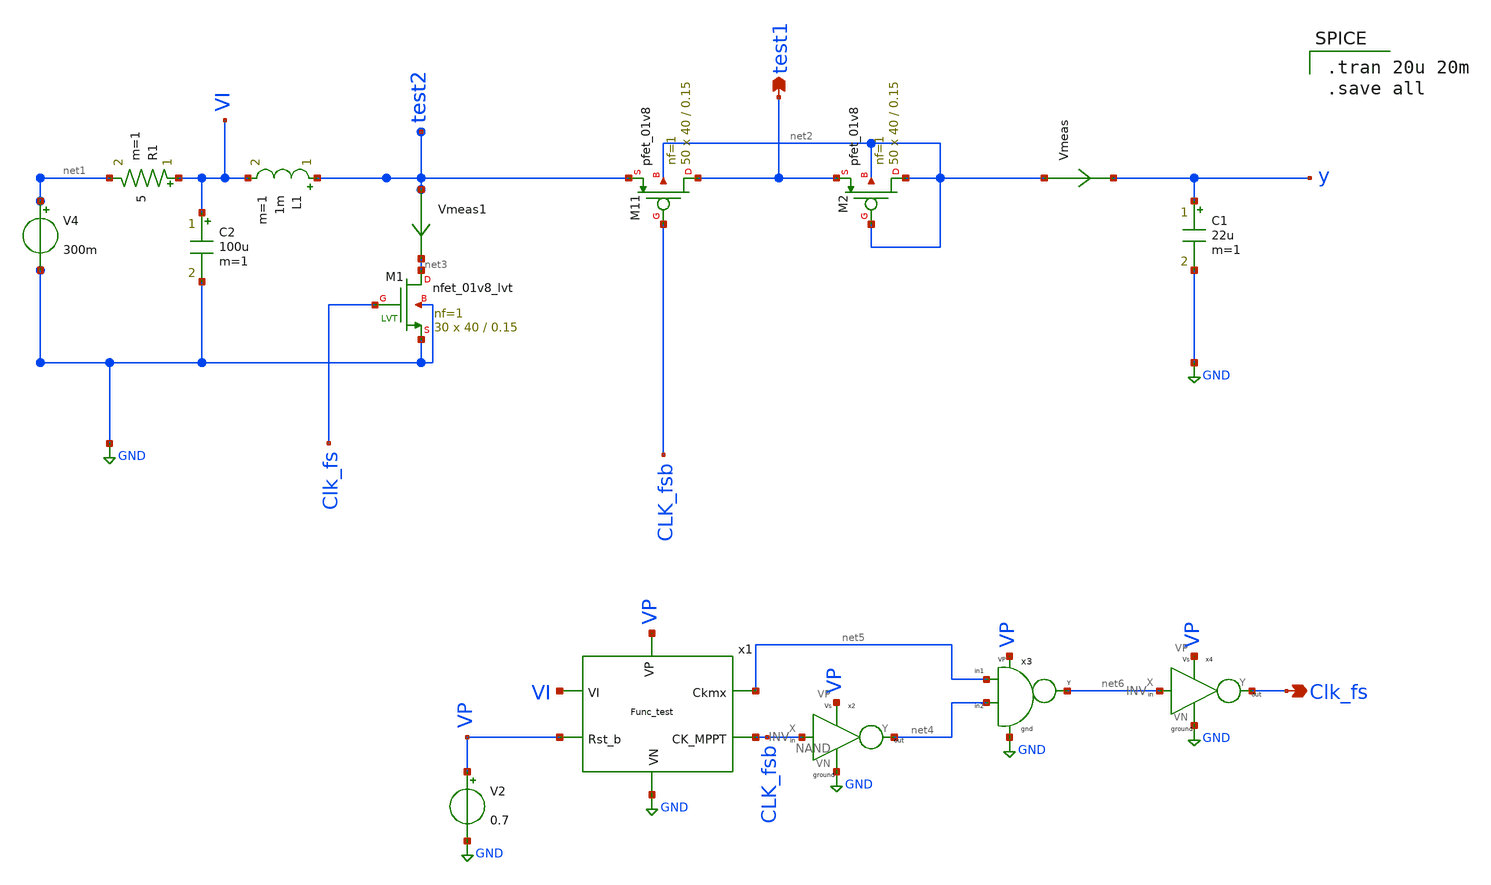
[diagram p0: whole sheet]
** sch_path: Blocks/MPPT/Functionality_test.sch
**.subckt Functionality_test test1 Clk_fs
*.opin test1
*.opin Clk_fs
C1 y GND 22u m=1
L1 test2 VI 1m m=1
XM11 test1 CLK_fsb test2 net2 sky130_fd_pr__pfet_01v8 L=0.15 W=40 nf=1 ad='int((nf+1)/2) * W/nf * 0.29'
+ as='int((nf+2)/2) * W/nf * 0.29' pd='2*int((nf+1)/2) * (W/nf + 0.29)' ps='2*int((nf+2)/2) * (W/nf + 0.29)'
+ nrd='0.29 / W' nrs='0.29 / W' sa=0 sb=0 sd=0 mult=50 m=50
Vmeas net2 y 0
.save i(vmeas)
Vmeas1 test2 net3 0
.save i(vmeas1)
XM2 net2 net2 test1 net2 sky130_fd_pr__pfet_01v8 L=0.15 W=40 nf=1 ad='int((nf+1)/2) * W/nf * 0.29' as='int((nf+2)/2) * W/nf * 0.29'
+ pd='2*int((nf+1)/2) * (W/nf + 0.29)' ps='2*int((nf+2)/2) * (W/nf + 0.29)' nrd='0.29 / W' nrs='0.29 / W'
+ sa=0 sb=0 sd=0 mult=50 m=50
XM1 net3 Clk_fs GND GND sky130_fd_pr__nfet_01v8_lvt L=0.15 W=40 nf=1 ad='int((nf+1)/2) * W/nf * 0.29'
+ as='int((nf+2)/2) * W/nf * 0.29' pd='2*int((nf+1)/2) * (W/nf + 0.29)' ps='2*int((nf+2)/2) * (W/nf + 0.29)'
+ nrd='0.29 / W' nrs='0.29 / W' sa=0 sb=0 sd=0 mult=30 m=30
R1 VI net1 5 m=1
C2 VI GND 100u m=1
x1 VI CLK_fsb net5 GND VP VP Func_test
x2 CLK_fsb net4 VP GND INV
x3 net4 net5 net6 VP GND NAND
x4 net6 Clk_fs VP GND INV
V2 VP GND 0.7
V4 net1 GND 300m
**** begin user architecture code

** opencircuitdesign pdks install
.lib $::SKYWATER_MODELS/sky130.lib.spice tt



.tran 20u 20m
.save all

**** end user architecture code
**.ends

* expanding   symbol:  pico_chipathon/Blocks/MPPT/Func_test.sym # of pins=6
** sym_path: Blocks/MPPT/Func_test.sym
** sch_path: Blocks/MPPT/Func_test.sch
.subckt Func_test VI CK_MPPT Ckmx VN Rst_b VP
*.ipin VI
*.ipin VP
*.ipin VN
*.ipin Rst_b
*.opin Ckmx
*.opin CK_MPPT
x1 VP net5 CK_MPPT Rst_b VN CK_MPPT1 CK_MPPT2 div8_copy
x2 net6 net5 VP VN Rst_b div32
x3 net7 CK_MPPT2 net4 Rst_b VN net11 VP net10 net8 net9 MPPT_Logic_Counter
x4 VP CK_MPPT1 VN net1 VI net11 net4 Conv_comp
R1 net1 net2 100k m=1
R2 net3 net1 100k m=1
C2 VI VN 0.1n m=1
C1 net1 VN 0.1n m=1
x5 net8 net7 net10 net9 VP VN net12 DCO
XM1 net3 CK_MPPT VN VN sky130_fd_pr__nfet_01v8_lvt L=0.15 W=0.42 nf=1 ad='int((nf+1)/2) * W/nf * 0.29'
+ as='int((nf+2)/2) * W/nf * 0.29' pd='2*int((nf+1)/2) * (W/nf + 0.29)' ps='2*int((nf+2)/2) * (W/nf + 0.29)'
+ nrd='0.29 / W' nrs='0.29 / W' sa=0 sb=0 sd=0 mult=50 m=50
XM2 net2 net13 VI VI sky130_fd_pr__pfet_01v8 L=0.15 W=1.26 nf=1 ad='int((nf+1)/2) * W/nf * 0.29' as='int((nf+2)/2) * W/nf * 0.29'
+ pd='2*int((nf+1)/2) * (W/nf + 0.29)' ps='2*int((nf+2)/2) * (W/nf + 0.29)' nrd='0.29 / W' nrs='0.29 / W'
+ sa=0 sb=0 sd=0 mult=50 m=50
x6 CK_MPPT net13 VP VN INV
x7 VP Ckmx net12 Rst_b VN div3
x8 Ckmx net6 VP VN Buff
.ends


* expanding   symbol:  pico_chipathon/component/INV/INV.sym # of pins=4
** sym_path: component/INV/INV.sym
** sch_path: component/INV/INV.sch
.subckt INV X Y VP VN
*.ipin X
*.opin Y
*.iopin VN
*.iopin VP
XM1 Y X VN VN sky130_fd_pr__nfet_01v8 L=0.15 W=0.42 nf=1 ad='int((nf+1)/2) * W/nf * 0.29' as='int((nf+2)/2) * W/nf * 0.29'
+ pd='2*int((nf+1)/2) * (W/nf + 0.29)' ps='2*int((nf+2)/2) * (W/nf + 0.29)' nrd='0.29 / W' nrs='0.29 / W'
+ sa=0 sb=0 sd=0 mult=1 m=1
XM2 Y X VP VP sky130_fd_pr__pfet_01v8 L=0.15 W=1.26 nf=1 ad='int((nf+1)/2) * W/nf * 0.29' as='int((nf+2)/2) * W/nf * 0.29'
+ pd='2*int((nf+1)/2) * (W/nf + 0.29)' ps='2*int((nf+2)/2) * (W/nf + 0.29)' nrd='0.29 / W' nrs='0.29 / W'
+ sa=0 sb=0 sd=0 mult=1 m=1
.ends


* expanding   symbol:  pico_chipathon/component/NAND2/NAND.sym # of pins=5
** sym_path: component/NAND2/NAND.sym
** sch_path: component/NAND2/NAND.sch
.subckt NAND B A Y VP VN
*.iopin VP
*.ipin A
*.ipin B
*.opin Y
*.iopin VN
XM1 Y A VP VP sky130_fd_pr__pfet_01v8 L=0.15 W=1.26 nf=1 ad='int((nf+1)/2) * W/nf * 0.29' as='int((nf+2)/2) * W/nf * 0.29'
+ pd='2*int((nf+1)/2) * (W/nf + 0.29)' ps='2*int((nf+2)/2) * (W/nf + 0.29)' nrd='0.29 / W' nrs='0.29 / W'
+ sa=0 sb=0 sd=0 mult=1 m=1
XM2 Y B VP VP sky130_fd_pr__pfet_01v8 L=0.15 W=1.26 nf=1 ad='int((nf+1)/2) * W/nf * 0.29' as='int((nf+2)/2) * W/nf * 0.29'
+ pd='2*int((nf+1)/2) * (W/nf + 0.29)' ps='2*int((nf+2)/2) * (W/nf + 0.29)' nrd='0.29 / W' nrs='0.29 / W'
+ sa=0 sb=0 sd=0 mult=1 m=1
XM3 Y A net1 net1 sky130_fd_pr__nfet_01v8 L=0.15 W=0.84 nf=1 ad='int((nf+1)/2) * W/nf * 0.29' as='int((nf+2)/2) * W/nf * 0.29'
+ pd='2*int((nf+1)/2) * (W/nf + 0.29)' ps='2*int((nf+2)/2) * (W/nf + 0.29)' nrd='0.29 / W' nrs='0.29 / W'
+ sa=0 sb=0 sd=0 mult=1 m=1
XM4 net1 B VN VN sky130_fd_pr__nfet_01v8 L=0.15 W=0.84 nf=1 ad='int((nf+1)/2) * W/nf * 0.29' as='int((nf+2)/2) * W/nf * 0.29'
+ pd='2*int((nf+1)/2) * (W/nf + 0.29)' ps='2*int((nf+2)/2) * (W/nf + 0.29)' nrd='0.29 / W' nrs='0.29 / W'
+ sa=0 sb=0 sd=0 mult=1 m=1
.ends


* expanding   symbol:  pico_chipathon/Blocks/MPPT/div8_copy.sym # of pins=7
** sym_path: Blocks/MPPT/div8_copy.sym
** sch_path: Blocks/MPPT/div8_copy.sch
.subckt div8_copy Vp Clk CK_MPPT RST_b Vn CK_MPPT1 CK_MPPT2
*.ipin Clk
*.ipin RST_b
*.opin CK_MPPT
*.opin CK_MPPT1
*.opin CK_MPPT2
*.ipin Vn
*.ipin Vp
x1 net2 Clk RST_b Vn Vp net1 net2 DFF1
x2 net3 net1 RST_b Vn Vp net4 net3 DFF1
x3 net6 net4 RST_b Vn Vp net5 net6 DFF1
x4 net7 CK_MPPT Vp Vn INV
x5 net8 CK_MPPT1 Vp Vn INV
x7 net9 CK_MPPT2 Vp Vn INV
x8 net1 net12 Vp Vn INV
x11 net4 net11 Vp Vn INV
x12 net4 net10 Vp Vn INV
x6 net5 net11 net12 Vp Vn net9 NAND3
x9 net5 net10 net1 Vp Vn net8 NAND3
x10 net5 net4 net1 Vp Vn net7 NAND3
.ends


* expanding   symbol:  pico_chipathon/Blocks/Divide by 32 ckt/div32.sym # of pins=5
** sym_path: Blocks/Divide by 32 ckt/div32.sym
** sch_path: Blocks/Divide by 32 ckt/div32.sch
.subckt div32 Clk Clk/32 VP VN RST_b
*.opin Clk/32
*.ipin Clk
*.iopin VP
*.iopin VN
*.ipin RST_b
x1 net2 Clk RST_b VN VP net1 net2 DFF1
x6 net9 net10 VN VP Buff
x2 net3 net1 RST_b VN VP net4 net3 DFF1
x3 net8 net4 RST_b VN VP net5 net8 DFF1
x4 net7 net5 RST_b VN VP net6 net7 DFF1
x5 net9 net6 RST_b VN VP Clk/32 net10 DFF1
.ends


* expanding   symbol:  pico_chipathon/Blocks/MPPT/MPPT_Logic_Counter.sym # of pins=10
** sym_path: Blocks/MPPT/MPPT_Logic_Counter.sym
** sch_path: Blocks/MPPT/MPPT_Logic_Counter.sch
.subckt MPPT_Logic_Counter QA Clk X_b Rst VN X VP QD QB QC
*.opin QD
*.ipin VP
*.opin QC
*.opin QB
*.opin QA
*.ipin VN
*.ipin X
*.ipin X_b
*.ipin Clk
*.ipin Rst
x4 net47 net46 net2 VP VN NAND
x5 QD X_b net38 VP VN NAND
x6 net51 net50 net3 VP VN NAND
x16 QA QD net29 VP VN NAND
x48 QB QD net31 VP VN NAND
x49 QC QD net32 VP VN NAND
x50 QD X net35 VP VN NAND
x52 net44 net43 net28 VP VN NAND
x54 VP net14 X_b QC QB_b QA_b VN nand4
x12 VP net15 X_b QD QB_b QA_b VN nand4
x15 VP net17 QD QC QB QA VN nand4
x22 VP net8 X QC_b QB QA VN nand4
x24 VP net36 X QC QB QA VN nand4
x17 VP net52 net53 net57 net50 VN nor3
x26 VP net54 net55 net56 net51 VN nor3
x56 VP net10 net11 net48 net46 VN nor3
x57 VP net49 net16 net18 net47 VN nor3
x25 VP net30 net33 net45 net43 VN nor3
x64 X_b QB QA VP VN net9 NAND3
x9 X QB_b QA VP VN net12 NAND3
x10 X QB QA_b VP VN net13 NAND3
x11 X_b QC QA VP VN net4 NAND3
x13 QC QB QA_b VP VN net5 NAND3
x14 QD QC QA VP VN net6 NAND3
x19 X QC QB_b VP VN net7 NAND3
x20 QC_b QB_b QA_b VP VN net39 NAND3
x23 VP net34 net37 net44 VN NOR2
x8 VP net38 net39 net56 VN NOR2
x1 net2 Clk Rst VN VP QB QB_b DFF1
x18 net3 Clk Rst VN VP QC QC_b DFF1
x29 net28 Clk Rst VN VP QD DFF
x32 net17 net18 VP VN INV
x38 net15 net16 VP VN INV
x39 net14 net49 VP VN INV
x40 net13 net48 VP VN INV
x42 net9 net10 VP VN INV
x43 net12 net11 VP VN INV
x31 net8 net55 VP VN INV
x33 net7 net54 VP VN INV
x36 net6 net57 VP VN INV
x37 net5 net53 VP VN INV
x41 net4 net52 VP VN INV
x34 net29 net30 VP VN INV
x44 net31 net33 VP VN INV
x51 net32 net45 VP VN INV
x53 net35 net34 VP VN INV
x55 net36 net37 VP VN INV
x35 net1 Clk Rst VN VP QA QA_b DFF1
x58 VP net20 net23 net42 net40 VN nor3
x59 VP net40 net41 net1 VN NOR2
x3 net27 net24 net41 VP VN NAND
x21 net19 net20 VP VN INV
x27 net21 net23 VP VN INV
x28 net22 net42 VP VN INV
x30 net25 net24 VP VN INV
x2 net26 net27 VP VN INV
x60 VP net26 X QD QC QB VN nand4
x7 QA_b QB net19 VP VN NAND
x45 QA_b QC net21 VP VN NAND
x46 QA_b QD net22 VP VN NAND
x47 QA_b X net25 VP VN NAND
.ends


* expanding   symbol:  pico_chipathon/Blocks/Conv_comparator/Conv_comp.sym # of pins=7
** sym_path: Blocks/Conv_comparator/Conv_comp.sym
** sch_path: Blocks/Conv_comparator/Conv_comp.sch
.subckt Conv_comp Vdd Clk VN Vin- Vin+ Out+ Out-
*.iopin Vin+
*.iopin Vin-
*.iopin Out+
*.iopin Out-
*.ipin VN
*.ipin Vdd
*.ipin Clk
XM6 net1 Clk Vdd Vdd sky130_fd_pr__pfet_01v8 L=0.15 W=1.26 nf=1 ad='int((nf+1)/2) * W/nf * 0.29' as='int((nf+2)/2) * W/nf * 0.29'
+ pd='2*int((nf+1)/2) * (W/nf + 0.29)' ps='2*int((nf+2)/2) * (W/nf + 0.29)' nrd='0.29 / W' nrs='0.29 / W'
+ sa=0 sb=0 sd=0 mult=1 m=1
XM7 O1- Vin+ net1 Vdd sky130_fd_pr__pfet_01v8 L=0.15 W=1.26 nf=1 ad='int((nf+1)/2) * W/nf * 0.29' as='int((nf+2)/2) * W/nf * 0.29'
+ pd='2*int((nf+1)/2) * (W/nf + 0.29)' ps='2*int((nf+2)/2) * (W/nf + 0.29)' nrd='0.29 / W' nrs='0.29 / W'
+ sa=0 sb=0 sd=0 mult=1 m=1
XM8 O1+ Vin- net1 Vdd sky130_fd_pr__pfet_01v8 L=0.15 W=1.26 nf=1 ad='int((nf+1)/2) * W/nf * 0.29' as='int((nf+2)/2) * W/nf * 0.29'
+ pd='2*int((nf+1)/2) * (W/nf + 0.29)' ps='2*int((nf+2)/2) * (W/nf + 0.29)' nrd='0.29 / W' nrs='0.29 / W'
+ sa=0 sb=0 sd=0 mult=1 m=1
XM5 O1- Clk VN VN sky130_fd_pr__nfet_01v8 L=0.15 W=0.42 nf=1 ad='int((nf+1)/2) * W/nf * 0.29' as='int((nf+2)/2) * W/nf * 0.29'
+ pd='2*int((nf+1)/2) * (W/nf + 0.29)' ps='2*int((nf+2)/2) * (W/nf + 0.29)' nrd='0.29 / W' nrs='0.29 / W'
+ sa=0 sb=0 sd=0 mult=1 m=1
XM21 O1+ Clk VN VN sky130_fd_pr__nfet_01v8 L=0.15 W=0.42 nf=1 ad='int((nf+1)/2) * W/nf * 0.29' as='int((nf+2)/2) * W/nf * 0.29'
+ pd='2*int((nf+1)/2) * (W/nf + 0.29)' ps='2*int((nf+2)/2) * (W/nf + 0.29)' nrd='0.29 / W' nrs='0.29 / W'
+ sa=0 sb=0 sd=0 mult=1 m=1
XM1 O2- Clk_b Vdd Vdd sky130_fd_pr__pfet_01v8 L=0.15 W=1.26 nf=1 ad='int((nf+1)/2) * W/nf * 0.29' as='int((nf+2)/2) * W/nf * 0.29'
+ pd='2*int((nf+1)/2) * (W/nf + 0.29)' ps='2*int((nf+2)/2) * (W/nf + 0.29)' nrd='0.29 / W' nrs='0.29 / W'
+ sa=0 sb=0 sd=0 mult=1 m=1
XM2 O2- O2+ Vdd Vdd sky130_fd_pr__pfet_01v8 L=0.15 W=1.26 nf=1 ad='int((nf+1)/2) * W/nf * 0.29' as='int((nf+2)/2) * W/nf * 0.29'
+ pd='2*int((nf+1)/2) * (W/nf + 0.29)' ps='2*int((nf+2)/2) * (W/nf + 0.29)' nrd='0.29 / W' nrs='0.29 / W'
+ sa=0 sb=0 sd=0 mult=1 m=1
XM3 O2+ O2- Vdd Vdd sky130_fd_pr__pfet_01v8 L=0.15 W=1.26 nf=1 ad='int((nf+1)/2) * W/nf * 0.29' as='int((nf+2)/2) * W/nf * 0.29'
+ pd='2*int((nf+1)/2) * (W/nf + 0.29)' ps='2*int((nf+2)/2) * (W/nf + 0.29)' nrd='0.29 / W' nrs='0.29 / W'
+ sa=0 sb=0 sd=0 mult=1 m=1
XM4 O2+ Clk_b Vdd Vdd sky130_fd_pr__pfet_01v8 L=0.15 W=1.26 nf=1 ad='int((nf+1)/2) * W/nf * 0.29' as='int((nf+2)/2) * W/nf * 0.29'
+ pd='2*int((nf+1)/2) * (W/nf + 0.29)' ps='2*int((nf+2)/2) * (W/nf + 0.29)' nrd='0.29 / W' nrs='0.29 / W'
+ sa=0 sb=0 sd=0 mult=1 m=1
XM9 net3 O1- O2- VN sky130_fd_pr__nfet_01v8 L=0.15 W=0.42 nf=1 ad='int((nf+1)/2) * W/nf * 0.29' as='int((nf+2)/2) * W/nf * 0.29'
+ pd='2*int((nf+1)/2) * (W/nf + 0.29)' ps='2*int((nf+2)/2) * (W/nf + 0.29)' nrd='0.29 / W' nrs='0.29 / W'
+ sa=0 sb=0 sd=0 mult=1 m=1
XM10 net2 O1+ O2+ VN sky130_fd_pr__nfet_01v8 L=0.15 W=0.42 nf=1 ad='int((nf+1)/2) * W/nf * 0.29' as='int((nf+2)/2) * W/nf * 0.29'
+ pd='2*int((nf+1)/2) * (W/nf + 0.29)' ps='2*int((nf+2)/2) * (W/nf + 0.29)' nrd='0.29 / W' nrs='0.29 / W'
+ sa=0 sb=0 sd=0 mult=1 m=1
XM11 VN O2+ net3 VN sky130_fd_pr__nfet_01v8 L=0.15 W=0.42 nf=1 ad='int((nf+1)/2) * W/nf * 0.29' as='int((nf+2)/2) * W/nf * 0.29'
+ pd='2*int((nf+1)/2) * (W/nf + 0.29)' ps='2*int((nf+2)/2) * (W/nf + 0.29)' nrd='0.29 / W' nrs='0.29 / W'
+ sa=0 sb=0 sd=0 mult=1 m=1
XM12 VN O2- net2 VN sky130_fd_pr__nfet_01v8 L=0.15 W=0.42 nf=1 ad='int((nf+1)/2) * W/nf * 0.29' as='int((nf+2)/2) * W/nf * 0.29'
+ pd='2*int((nf+1)/2) * (W/nf + 0.29)' ps='2*int((nf+2)/2) * (W/nf + 0.29)' nrd='0.29 / W' nrs='0.29 / W'
+ sa=0 sb=0 sd=0 mult=1 m=1
x1 Clk Clk_b Vdd VN INV
x2 O2+ net4 Vdd VN INV
x3 O2- net5 Vdd VN INV
x4 net4 Clk Vdd VN Vdd Out+ DFF
x5 net5 Clk Vdd VN Vdd Out- DFF
.ends


* expanding   symbol:  pico_chipathon/Blocks/DCO/DCO.sym # of pins=7
** sym_path: Blocks/DCO/DCO.sym
** sch_path: Blocks/DCO/DCO.sch
.subckt DCO Y1 Y0 Y3 Y2 VS VN Out
*.ipin VS
*.opin Out
*.ipin VN
*.iopin Y3
*.iopin Y2
*.iopin Y1
*.iopin Y0
C1 net38 VN 5f m=1
C2 net39 VN 5f m=1
C3 net40 VN 5f m=1
C4 net41 VN 5f m=1
XM1 net16 L0 net38 VN sky130_fd_pr__nfet_01v8 L=0.15 W=5 nf=1 ad='int((nf+1)/2) * W/nf * 0.29' as='int((nf+2)/2) * W/nf * 0.29'
+ pd='2*int((nf+1)/2) * (W/nf + 0.29)' ps='2*int((nf+2)/2) * (W/nf + 0.29)' nrd='0.29 / W' nrs='0.29 / W'
+ sa=0 sb=0 sd=0 mult=1 m=1
XM2 net17 L1 net39 VN sky130_fd_pr__nfet_01v8 L=0.15 W=5 nf=1 ad='int((nf+1)/2) * W/nf * 0.29' as='int((nf+2)/2) * W/nf * 0.29'
+ pd='2*int((nf+1)/2) * (W/nf + 0.29)' ps='2*int((nf+2)/2) * (W/nf + 0.29)' nrd='0.29 / W' nrs='0.29 / W'
+ sa=0 sb=0 sd=0 mult=1 m=1
XM3 net18 L2 net40 VN sky130_fd_pr__nfet_01v8 L=0.15 W=5 nf=1 ad='int((nf+1)/2) * W/nf * 0.29' as='int((nf+2)/2) * W/nf * 0.29'
+ pd='2*int((nf+1)/2) * (W/nf + 0.29)' ps='2*int((nf+2)/2) * (W/nf + 0.29)' nrd='0.29 / W' nrs='0.29 / W'
+ sa=0 sb=0 sd=0 mult=1 m=1
XM4 net19 L3 net41 VN sky130_fd_pr__nfet_01v8 L=0.15 W=5 nf=1 ad='int((nf+1)/2) * W/nf * 0.29' as='int((nf+2)/2) * W/nf * 0.29'
+ pd='2*int((nf+1)/2) * (W/nf + 0.29)' ps='2*int((nf+2)/2) * (W/nf + 0.29)' nrd='0.29 / W' nrs='0.29 / W'
+ sa=0 sb=0 sd=0 mult=1 m=1
XM5 net33 H0 net17 VN sky130_fd_pr__nfet_01v8 L=0.15 W=10 nf=1 ad='int((nf+1)/2) * W/nf * 0.29' as='int((nf+2)/2) * W/nf * 0.29'
+ pd='2*int((nf+1)/2) * (W/nf + 0.29)' ps='2*int((nf+2)/2) * (W/nf + 0.29)' nrd='0.29 / W' nrs='0.29 / W'
+ sa=0 sb=0 sd=0 mult=1 m=1
XM6 net33 H1 net19 VN sky130_fd_pr__nfet_01v8 L=0.15 W=10 nf=1 ad='int((nf+1)/2) * W/nf * 0.29' as='int((nf+2)/2) * W/nf * 0.29'
+ pd='2*int((nf+1)/2) * (W/nf + 0.29)' ps='2*int((nf+2)/2) * (W/nf + 0.29)' nrd='0.29 / W' nrs='0.29 / W'
+ sa=0 sb=0 sd=0 mult=1 m=1
XM7 net33 H2 net21 VN sky130_fd_pr__nfet_01v8 L=0.15 W=10 nf=1 ad='int((nf+1)/2) * W/nf * 0.29' as='int((nf+2)/2) * W/nf * 0.29'
+ pd='2*int((nf+1)/2) * (W/nf + 0.29)' ps='2*int((nf+2)/2) * (W/nf + 0.29)' nrd='0.29 / W' nrs='0.29 / W'
+ sa=0 sb=0 sd=0 mult=1 m=1
XM9 net33 net36 net17 VS sky130_fd_pr__pfet_01v8 L=0.15 W=3 nf=1 ad='int((nf+1)/2) * W/nf * 0.29' as='int((nf+2)/2) * W/nf * 0.29'
+ pd='2*int((nf+1)/2) * (W/nf + 0.29)' ps='2*int((nf+2)/2) * (W/nf + 0.29)' nrd='0.29 / W' nrs='0.29 / W'
+ sa=0 sb=0 sd=0 mult=1 m=1
XM10 net33 net34 net19 VS sky130_fd_pr__pfet_01v8 L=0.15 W=3 nf=1 ad='int((nf+1)/2) * W/nf * 0.29' as='int((nf+2)/2) * W/nf * 0.29'
+ pd='2*int((nf+1)/2) * (W/nf + 0.29)' ps='2*int((nf+2)/2) * (W/nf + 0.29)' nrd='0.29 / W' nrs='0.29 / W'
+ sa=0 sb=0 sd=0 mult=1 m=1
XM11 net33 net35 net21 VS sky130_fd_pr__pfet_01v8 L=0.15 W=3 nf=1 ad='int((nf+1)/2) * W/nf * 0.29' as='int((nf+2)/2) * W/nf * 0.29'
+ pd='2*int((nf+1)/2) * (W/nf + 0.29)' ps='2*int((nf+2)/2) * (W/nf + 0.29)' nrd='0.29 / W' nrs='0.29 / W'
+ sa=0 sb=0 sd=0 mult=1 m=1
XM8 net33 net37 Out VS sky130_fd_pr__pfet_01v8 L=0.15 W=3 nf=1 ad='int((nf+1)/2) * W/nf * 0.29' as='int((nf+2)/2) * W/nf * 0.29'
+ pd='2*int((nf+1)/2) * (W/nf + 0.29)' ps='2*int((nf+2)/2) * (W/nf + 0.29)' nrd='0.29 / W' nrs='0.29 / W'
+ sa=0 sb=0 sd=0 mult=1 m=1
XM12 net33 H3 Out VN sky130_fd_pr__nfet_01v8 L=0.15 W=10 nf=1 ad='int((nf+1)/2) * W/nf * 0.29' as='int((nf+2)/2) * W/nf * 0.29'
+ pd='2*int((nf+1)/2) * (W/nf + 0.29)' ps='2*int((nf+2)/2) * (W/nf + 0.29)' nrd='0.29 / W' nrs='0.29 / W'
+ sa=0 sb=0 sd=0 mult=1 m=1
XM13 net16 net45 net38 VS sky130_fd_pr__pfet_01v8 L=0.15 W=3 nf=1 ad='int((nf+1)/2) * W/nf * 0.29' as='int((nf+2)/2) * W/nf * 0.29'
+ pd='2*int((nf+1)/2) * (W/nf + 0.29)' ps='2*int((nf+2)/2) * (W/nf + 0.29)' nrd='0.29 / W' nrs='0.29 / W'
+ sa=0 sb=0 sd=0 mult=1 m=1
XM14 net17 net44 net39 VS sky130_fd_pr__pfet_01v8 L=0.15 W=3 nf=1 ad='int((nf+1)/2) * W/nf * 0.29' as='int((nf+2)/2) * W/nf * 0.29'
+ pd='2*int((nf+1)/2) * (W/nf + 0.29)' ps='2*int((nf+2)/2) * (W/nf + 0.29)' nrd='0.29 / W' nrs='0.29 / W'
+ sa=0 sb=0 sd=0 mult=1 m=1
XM15 net18 net42 net40 VS sky130_fd_pr__pfet_01v8 L=0.15 W=3 nf=1 ad='int((nf+1)/2) * W/nf * 0.29' as='int((nf+2)/2) * W/nf * 0.29'
+ pd='2*int((nf+1)/2) * (W/nf + 0.29)' ps='2*int((nf+2)/2) * (W/nf + 0.29)' nrd='0.29 / W' nrs='0.29 / W'
+ sa=0 sb=0 sd=0 mult=1 m=1
XM16 net19 net43 net41 VS sky130_fd_pr__pfet_01v8 L=0.15 W=3 nf=1 ad='int((nf+1)/2) * W/nf * 0.29' as='int((nf+2)/2) * W/nf * 0.29'
+ pd='2*int((nf+1)/2) * (W/nf + 0.29)' ps='2*int((nf+2)/2) * (W/nf + 0.29)' nrd='0.29 / W' nrs='0.29 / W'
+ sa=0 sb=0 sd=0 mult=1 m=1
x9 Y3 net1 VS VN INV_a
x10 net46 H0 VS VN INV_a
x11 net47 H1 VS VN INV_a
x13 net48 H2 VS VN INV_a
x15 net49 H3 VS VN INV_a
x17 Y2 net4 VS VN INV_a
x18 Y3 net3 VS VN INV_a
x19 Y2 net2 VS VN INV_a
x23 H3 net37 VS VN INV_a
x3 H2 net35 VS VN INV_a
x2 H1 net34 VS VN INV_a
x1 H0 net36 VS VN INV_a
x4 L0 net45 VS VN INV_a
x20 L1 net44 VS VN INV_a
x5 L2 net42 VS VN INV_a
x6 L3 net43 VS VN INV_a
x7 Y1 net11 VS VN INV_a
x8 net50 net9 VS VN INV_a
x21 net51 net10 VS VN INV_a
x22 net52 L0 VS VN INV_a
x24 net53 net12 VS VN INV_a
x26 Y0 net14 VS VN INV_a
x34 net54 net13 VS VN INV_a
x28 net55 L1 VS VN INV_a
x36 Y0 net11 net50 VS VN NAND
x38 net14 Y1 net53 VS VN NAND
x33 Y0 Y1 net51 VS VN NAND
x37 net6 net5 net52 VS VN NAND
x25 net8 net7 net55 VS VN NAND
x27 Y0 Y1 net54 VS VN NAND
x39 Y1 net29 VS VN INV_a
x40 net56 net27 VS VN INV_a
x41 net57 net30 VS VN INV_a
x42 net58 L3 VS VN INV_a
x43 net59 L2 VS VN INV_a
x44 net60 net31 VS VN INV_a
x55 Y0 net32 VS VN INV_a
x59 net61 net28 VS VN INV_a
x62 Y0 net29 net56 VS VN NAND
x63 Y0 Y1 net61 VS VN NAND
x64 net32 Y1 net57 VS VN NAND
x65 Y0 Y1 net60 VS VN NAND
x66 net24 net23 net59 VS VN NAND
x67 net26 net25 net58 VS VN NAND
x54 net31 net30 net25 VS VN OR_2
x58 H3 H2 net26 VS VN OR_2
x60 net28 net27 net23 VS VN OR_2
x68 H3 H2 net24 VS VN OR_2
x32 H1 H0 net8 VS VN OR_2
x31 net13 net12 net7 VS VN OR_2
x56 H1 H0 net6 VS VN OR_2
x30 net10 net9 net5 VS VN OR_2
x29 net2 net1 net46 VS VN NAND
x57 net3 Y2 net47 VS VN NAND
x61 net4 Y3 net48 VS VN NAND
x69 Y2 Y3 net49 VS VN NAND
x12 net33 net15 VS VN Redn_INV
x14 net15 net16 VS VN Redn_INV
x16 net16 net17 VS VN Redn_INV
x35 net17 net18 VS VN Redn_INV
x53 net18 net19 VS VN Redn_INV
x70 net19 net20 VS VN Redn_INV
x71 net20 net21 VS VN Redn_INV
x72 net21 net22 VS VN Redn_INV
x73 net22 Out VS VN Redn_INV
.ends


* expanding   symbol:  pico_chipathon/Blocks/Divide by 3 Circuit/div3.sym # of pins=5
** sym_path: Blocks/Divide by 3 Circuit/div3.sym
** sch_path: Blocks/Divide by 3 Circuit/div3.sch
.subckt div3 VP Clk/3 Clk RST_b VN
*.opin Clk/3
*.ipin Clk
*.ipin VN
*.ipin RST_b
*.ipin VP
x3 net2 Clk RST_b VN VP net3 net5 DFF1
x8 Clk net1 VP VN INV
x1 net8 net2 VP VN INV
x9 net6 net5 net8 VP VN NAND
x2 net7 net4 Clk/3 VP VN OR_2
x7 net3 Clk RST_b VN VP net4 net6 DFF1
x10 net4 net1 RST_b VN VP net7 net9 DFF1
.ends


* expanding   symbol:  pico_chipathon/Blocks/Buffer/Buff.sym # of pins=4
** sym_path: Blocks/Buffer/Buff.sym
** sch_path: Blocks/Buffer/Buff.sch
.subckt Buff X Y VP VN
*.ipin X
*.opin Y
*.iopin VN
*.iopin VP
x1 X net1 VP VN INV
x2 net1 Y VP VN INV
.ends


* expanding   symbol:  component/FlipFlops/DFF1.sym # of pins=7
** sym_path: component/FlipFlops/DFF1.sym
** sch_path: component/FlipFlops/DFF1.sch
.subckt DFF1 D Clk RST VN VP Q Qb
*.opin Q
*.iopin VN
*.iopin VP
*.ipin Clk
*.ipin D
*.ipin RST
*.opin Qb
x7 net2 net4 net3 VP VN NAND
x8 net3 Clk RST VP VN net2 NAND3
x6 Q net1 RST VP VN Qb NAND3
x4 net2 Clk net4 VP VN net1 NAND3
x5 net1 D RST VP VN net4 NAND3
x1 Qb net2 Q VP VN NAND
.ends


* expanding   symbol:  component/NAND3/NAND3.sym # of pins=6
** sym_path: component/NAND3/NAND3.sym
** sch_path: component/NAND3/NAND3.sch
.subckt NAND3 A B C VP VN Y
*.iopin VP
*.iopin VN
*.ipin A
*.ipin B
*.ipin C
*.opin Y
XM1 Y A net1 VN sky130_fd_pr__nfet_01v8 L=0.15 W=1.26 nf=1 ad='int((nf+1)/2) * W/nf * 0.29' as='int((nf+2)/2) * W/nf * 0.29'
+ pd='2*int((nf+1)/2) * (W/nf + 0.29)' ps='2*int((nf+2)/2) * (W/nf + 0.29)' nrd='0.29 / W' nrs='0.29 / W'
+ sa=0 sb=0 sd=0 mult=1 m=1
XM2 net1 B net2 VN sky130_fd_pr__nfet_01v8 L=0.15 W=1.26 nf=1 ad='int((nf+1)/2) * W/nf * 0.29' as='int((nf+2)/2) * W/nf * 0.29'
+ pd='2*int((nf+1)/2) * (W/nf + 0.29)' ps='2*int((nf+2)/2) * (W/nf + 0.29)' nrd='0.29 / W' nrs='0.29 / W'
+ sa=0 sb=0 sd=0 mult=1 m=1
XM3 net2 C VN VN sky130_fd_pr__nfet_01v8 L=0.15 W=1.26 nf=1 ad='int((nf+1)/2) * W/nf * 0.29' as='int((nf+2)/2) * W/nf * 0.29'
+ pd='2*int((nf+1)/2) * (W/nf + 0.29)' ps='2*int((nf+2)/2) * (W/nf + 0.29)' nrd='0.29 / W' nrs='0.29 / W'
+ sa=0 sb=0 sd=0 mult=1 m=1
XM4 Y A VP VP sky130_fd_pr__pfet_01v8 L=0.15 W=1.26 nf=1 ad='int((nf+1)/2) * W/nf * 0.29' as='int((nf+2)/2) * W/nf * 0.29'
+ pd='2*int((nf+1)/2) * (W/nf + 0.29)' ps='2*int((nf+2)/2) * (W/nf + 0.29)' nrd='0.29 / W' nrs='0.29 / W'
+ sa=0 sb=0 sd=0 mult=1 m=1
XM5 Y B VP VP sky130_fd_pr__pfet_01v8 L=0.15 W=1.26 nf=1 ad='int((nf+1)/2) * W/nf * 0.29' as='int((nf+2)/2) * W/nf * 0.29'
+ pd='2*int((nf+1)/2) * (W/nf + 0.29)' ps='2*int((nf+2)/2) * (W/nf + 0.29)' nrd='0.29 / W' nrs='0.29 / W'
+ sa=0 sb=0 sd=0 mult=1 m=1
XM6 Y C VP VP sky130_fd_pr__pfet_01v8 L=0.15 W=1.26 nf=1 ad='int((nf+1)/2) * W/nf * 0.29' as='int((nf+2)/2) * W/nf * 0.29'
+ pd='2*int((nf+1)/2) * (W/nf + 0.29)' ps='2*int((nf+2)/2) * (W/nf + 0.29)' nrd='0.29 / W' nrs='0.29 / W'
+ sa=0 sb=0 sd=0 mult=1 m=1
.ends


* expanding   symbol:  pico_chipathon/component/NAND4/nand4.sym # of pins=7
** sym_path: component/NAND4/nand4.sym
** sch_path: component/NAND4/nand4.sch
.subckt nand4 VP Y A B C D VN
*.ipin A
*.ipin B
*.ipin C
*.opin Y
*.ipin D
*.ipin VP
*.ipin VN
XM1 Y A net1 VN sky130_fd_pr__nfet_01v8 L=0.15 W=1.68 nf=1 ad='int((nf+1)/2) * W/nf * 0.29' as='int((nf+2)/2) * W/nf * 0.29'
+ pd='2*int((nf+1)/2) * (W/nf + 0.29)' ps='2*int((nf+2)/2) * (W/nf + 0.29)' nrd='0.29 / W' nrs='0.29 / W'
+ sa=0 sb=0 sd=0 mult=1 m=1
XM2 net1 B net2 VN sky130_fd_pr__nfet_01v8 L=0.15 W=1.68 nf=1 ad='int((nf+1)/2) * W/nf * 0.29' as='int((nf+2)/2) * W/nf * 0.29'
+ pd='2*int((nf+1)/2) * (W/nf + 0.29)' ps='2*int((nf+2)/2) * (W/nf + 0.29)' nrd='0.29 / W' nrs='0.29 / W'
+ sa=0 sb=0 sd=0 mult=1 m=1
XM3 net2 C net3 VN sky130_fd_pr__nfet_01v8 L=0.15 W=1.68 nf=1 ad='int((nf+1)/2) * W/nf * 0.29' as='int((nf+2)/2) * W/nf * 0.29'
+ pd='2*int((nf+1)/2) * (W/nf + 0.29)' ps='2*int((nf+2)/2) * (W/nf + 0.29)' nrd='0.29 / W' nrs='0.29 / W'
+ sa=0 sb=0 sd=0 mult=1 m=1
XM4 Y A VP VP sky130_fd_pr__pfet_01v8 L=0.15 W=1.26 nf=1 ad='int((nf+1)/2) * W/nf * 0.29' as='int((nf+2)/2) * W/nf * 0.29'
+ pd='2*int((nf+1)/2) * (W/nf + 0.29)' ps='2*int((nf+2)/2) * (W/nf + 0.29)' nrd='0.29 / W' nrs='0.29 / W'
+ sa=0 sb=0 sd=0 mult=1 m=1
XM5 Y B VP VP sky130_fd_pr__pfet_01v8 L=0.15 W=1.26 nf=1 ad='int((nf+1)/2) * W/nf * 0.29' as='int((nf+2)/2) * W/nf * 0.29'
+ pd='2*int((nf+1)/2) * (W/nf + 0.29)' ps='2*int((nf+2)/2) * (W/nf + 0.29)' nrd='0.29 / W' nrs='0.29 / W'
+ sa=0 sb=0 sd=0 mult=1 m=1
XM6 Y C VP VP sky130_fd_pr__pfet_01v8 L=0.15 W=1.26 nf=1 ad='int((nf+1)/2) * W/nf * 0.29' as='int((nf+2)/2) * W/nf * 0.29'
+ pd='2*int((nf+1)/2) * (W/nf + 0.29)' ps='2*int((nf+2)/2) * (W/nf + 0.29)' nrd='0.29 / W' nrs='0.29 / W'
+ sa=0 sb=0 sd=0 mult=1 m=1
XM7 Y D VP VP sky130_fd_pr__pfet_01v8 L=0.15 W=1.26 nf=1 ad='int((nf+1)/2) * W/nf * 0.29' as='int((nf+2)/2) * W/nf * 0.29'
+ pd='2*int((nf+1)/2) * (W/nf + 0.29)' ps='2*int((nf+2)/2) * (W/nf + 0.29)' nrd='0.29 / W' nrs='0.29 / W'
+ sa=0 sb=0 sd=0 mult=1 m=1
XM8 net3 D VN VN sky130_fd_pr__nfet_01v8 L=0.15 W=1.68 nf=1 ad='int((nf+1)/2) * W/nf * 0.29' as='int((nf+2)/2) * W/nf * 0.29'
+ pd='2*int((nf+1)/2) * (W/nf + 0.29)' ps='2*int((nf+2)/2) * (W/nf + 0.29)' nrd='0.29 / W' nrs='0.29 / W'
+ sa=0 sb=0 sd=0 mult=1 m=1
.ends


* expanding   symbol:  pico_chipathon/component/NOR3/nor3.sym # of pins=6
** sym_path: component/NOR3/nor3.sym
** sch_path: component/NOR3/nor3.sch
.subckt nor3 VP A B C Y VN
*.opin Y
*.ipin C
*.ipin A
*.ipin B
*.ipin VP
*.ipin VN
XM5 Y B VN VN sky130_fd_pr__nfet_01v8 L=0.15 W=0.42 nf=1 ad='int((nf+1)/2) * W/nf * 0.29' as='int((nf+2)/2) * W/nf * 0.29'
+ pd='2*int((nf+1)/2) * (W/nf + 0.29)' ps='2*int((nf+2)/2) * (W/nf + 0.29)' nrd='0.29 / W' nrs='0.29 / W'
+ sa=0 sb=0 sd=0 mult=1 m=1
XM3 Y A VN VN sky130_fd_pr__nfet_01v8 L=0.15 W=0.42 nf=1 ad='int((nf+1)/2) * W/nf * 0.29' as='int((nf+2)/2) * W/nf * 0.29'
+ pd='2*int((nf+1)/2) * (W/nf + 0.29)' ps='2*int((nf+2)/2) * (W/nf + 0.29)' nrd='0.29 / W' nrs='0.29 / W'
+ sa=0 sb=0 sd=0 mult=1 m=1
XM2 Y C net2 VP sky130_fd_pr__pfet_01v8 L=0.15 W=3.78 nf=1 ad='int((nf+1)/2) * W/nf * 0.29' as='int((nf+2)/2) * W/nf * 0.29'
+ pd='2*int((nf+1)/2) * (W/nf + 0.29)' ps='2*int((nf+2)/2) * (W/nf + 0.29)' nrd='0.29 / W' nrs='0.29 / W'
+ sa=0 sb=0 sd=0 mult=1 m=1
XM1 net1 A VP VP sky130_fd_pr__pfet_01v8 L=0.15 W=3.78 nf=1 ad='int((nf+1)/2) * W/nf * 0.29' as='int((nf+2)/2) * W/nf * 0.29'
+ pd='2*int((nf+1)/2) * (W/nf + 0.29)' ps='2*int((nf+2)/2) * (W/nf + 0.29)' nrd='0.29 / W' nrs='0.29 / W'
+ sa=0 sb=0 sd=0 mult=1 m=1
XM6 net2 B net1 VP sky130_fd_pr__pfet_01v8 L=0.15 W=3.78 nf=1 ad='int((nf+1)/2) * W/nf * 0.29' as='int((nf+2)/2) * W/nf * 0.29'
+ pd='2*int((nf+1)/2) * (W/nf + 0.29)' ps='2*int((nf+2)/2) * (W/nf + 0.29)' nrd='0.29 / W' nrs='0.29 / W'
+ sa=0 sb=0 sd=0 mult=1 m=1
XM8 Y C VN VN sky130_fd_pr__nfet_01v8 L=0.15 W=0.42 nf=1 ad='int((nf+1)/2) * W/nf * 0.29' as='int((nf+2)/2) * W/nf * 0.29'
+ pd='2*int((nf+1)/2) * (W/nf + 0.29)' ps='2*int((nf+2)/2) * (W/nf + 0.29)' nrd='0.29 / W' nrs='0.29 / W'
+ sa=0 sb=0 sd=0 mult=1 m=1
.ends


* expanding   symbol:  pico_chipathon/component/NOR2/NOR2.sym # of pins=5
** sym_path: component/NOR2/NOR2.sym
** sch_path: component/NOR2/NOR2.sch
.subckt NOR2 VP A B Y VN
*.opin Y
*.ipin A
*.ipin B
*.ipin VP
*.ipin VN
XM5 Y B VN VN sky130_fd_pr__nfet_01v8 L=0.15 W=0.42 nf=1 ad='int((nf+1)/2) * W/nf * 0.29' as='int((nf+2)/2) * W/nf * 0.29'
+ pd='2*int((nf+1)/2) * (W/nf + 0.29)' ps='2*int((nf+2)/2) * (W/nf + 0.29)' nrd='0.29 / W' nrs='0.29 / W'
+ sa=0 sb=0 sd=0 mult=1 m=1
XM3 Y A VN VN sky130_fd_pr__nfet_01v8 L=0.15 W=0.42 nf=1 ad='int((nf+1)/2) * W/nf * 0.29' as='int((nf+2)/2) * W/nf * 0.29'
+ pd='2*int((nf+1)/2) * (W/nf + 0.29)' ps='2*int((nf+2)/2) * (W/nf + 0.29)' nrd='0.29 / W' nrs='0.29 / W'
+ sa=0 sb=0 sd=0 mult=1 m=1
XM2 net1 A VP VP sky130_fd_pr__pfet_01v8 L=0.15 W=2.52 nf=1 ad='int((nf+1)/2) * W/nf * 0.29' as='int((nf+2)/2) * W/nf * 0.29'
+ pd='2*int((nf+1)/2) * (W/nf + 0.29)' ps='2*int((nf+2)/2) * (W/nf + 0.29)' nrd='0.29 / W' nrs='0.29 / W'
+ sa=0 sb=0 sd=0 mult=1 m=1
XM4 Y B net1 VP sky130_fd_pr__pfet_01v8 L=0.15 W=2.52 nf=1 ad='int((nf+1)/2) * W/nf * 0.29' as='int((nf+2)/2) * W/nf * 0.29'
+ pd='2*int((nf+1)/2) * (W/nf + 0.29)' ps='2*int((nf+2)/2) * (W/nf + 0.29)' nrd='0.29 / W' nrs='0.29 / W'
+ sa=0 sb=0 sd=0 mult=1 m=1
.ends


* expanding   symbol:  pico_chipathon/component/FlipFlops/DFF.sym # of pins=6
** sym_path: component/FlipFlops/DFF.sym
** sch_path: component/FlipFlops/DFF.sch
.subckt DFF D Clk RST VN VP Q
*.opin Q
*.iopin VN
*.iopin VP
*.ipin Clk
*.ipin D
*.ipin RST
x1 net2 net5 net4 VP VN NAND
x7 net4 Clk RST VP VN net2 NAND3
x3 Q net1 RST VP VN net3 NAND3
x4 net2 Clk net5 VP VN net1 NAND3
x5 net1 D RST VP VN net5 NAND3
x6 net3 net2 Q VP VN NAND
.ends


* expanding   symbol:  pico_chipathon/component/INV/INV_a.sym # of pins=4
** sym_path: component/INV/INV_a.sym
** sch_path: component/INV/INV_a.sch
.subckt INV_a X Y VP VN
*.ipin X
*.opin Y
*.iopin VP
*.iopin VN
XM1 Y X VN VN sky130_fd_pr__nfet_01v8 L=0.15 W=1 nf=1 ad='int((nf+1)/2) * W/nf * 0.29' as='int((nf+2)/2) * W/nf * 0.29'
+ pd='2*int((nf+1)/2) * (W/nf + 0.29)' ps='2*int((nf+2)/2) * (W/nf + 0.29)' nrd='0.29 / W' nrs='0.29 / W'
+ sa=0 sb=0 sd=0 mult=1 m=1
XM2 Y X VP VP sky130_fd_pr__pfet_01v8 L=0.15 W=3 nf=1 ad='int((nf+1)/2) * W/nf * 0.29' as='int((nf+2)/2) * W/nf * 0.29'
+ pd='2*int((nf+1)/2) * (W/nf + 0.29)' ps='2*int((nf+2)/2) * (W/nf + 0.29)' nrd='0.29 / W' nrs='0.29 / W'
+ sa=0 sb=0 sd=0 mult=1 m=1
.ends


* expanding   symbol:  pico_chipathon/component/OR2/OR_2.sym # of pins=5
** sym_path: component/OR2/OR_2.sym
** sch_path: component/OR2/OR_2.sch
.subckt OR_2 B A Y VP VN
*.iopin VP
*.iopin VN
*.ipin A
*.ipin B
*.opin Y
XM1 net1 B VN VN sky130_fd_pr__nfet_01v8 L=0.15 W=0.42 nf=1 ad='int((nf+1)/2) * W/nf * 0.29' as='int((nf+2)/2) * W/nf * 0.29'
+ pd='2*int((nf+1)/2) * (W/nf + 0.29)' ps='2*int((nf+2)/2) * (W/nf + 0.29)' nrd='0.29 / W' nrs='0.29 / W'
+ sa=0 sb=0 sd=0 mult=1 m=1
XM2 net1 A VN VN sky130_fd_pr__nfet_01v8 L=0.15 W=0.42 nf=1 ad='int((nf+1)/2) * W/nf * 0.29' as='int((nf+2)/2) * W/nf * 0.29'
+ pd='2*int((nf+1)/2) * (W/nf + 0.29)' ps='2*int((nf+2)/2) * (W/nf + 0.29)' nrd='0.29 / W' nrs='0.29 / W'
+ sa=0 sb=0 sd=0 mult=1 m=1
XM3 net1 B net2 VP sky130_fd_pr__pfet_01v8 L=0.15 W=2.52 nf=1 ad='int((nf+1)/2) * W/nf * 0.29' as='int((nf+2)/2) * W/nf * 0.29'
+ pd='2*int((nf+1)/2) * (W/nf + 0.29)' ps='2*int((nf+2)/2) * (W/nf + 0.29)' nrd='0.29 / W' nrs='0.29 / W'
+ sa=0 sb=0 sd=0 mult=1 m=1
XM4 net2 A VP VP sky130_fd_pr__pfet_01v8 L=0.15 W=2.52 nf=1 ad='int((nf+1)/2) * W/nf * 0.29' as='int((nf+2)/2) * W/nf * 0.29'
+ pd='2*int((nf+1)/2) * (W/nf + 0.29)' ps='2*int((nf+2)/2) * (W/nf + 0.29)' nrd='0.29 / W' nrs='0.29 / W'
+ sa=0 sb=0 sd=0 mult=1 m=1
x1 net1 Y VP VN INV
.ends


* expanding   symbol:  pico_chipathon/component/Reduntant_Inverter/Redn_INV.sym # of pins=4
** sym_path: component/Reduntant_Inverter/Redn_INV.sym
** sch_path: component/Reduntant_Inverter/Redn_INV.sch
.subckt Redn_INV X Y VP VN
*.opin Y
*.ipin X
*.iopin VP
*.iopin VN
XM15 net4 X VN VN sky130_fd_pr__nfet_01v8_lvt L=0.15 W=1 nf=1 ad='int((nf+1)/2) * W/nf * 0.29' as='int((nf+2)/2) * W/nf * 0.29'
+ pd='2*int((nf+1)/2) * (W/nf + 0.29)' ps='2*int((nf+2)/2) * (W/nf + 0.29)' nrd='0.29 / W' nrs='0.29 / W'
+ sa=0 sb=0 sd=0 mult=1 m=1
XM1 net5 X net3 VN sky130_fd_pr__nfet_01v8_lvt L=0.15 W=3.25 nf=1 ad='int((nf+1)/2) * W/nf * 0.29' as='int((nf+2)/2) * W/nf * 0.29'
+ pd='2*int((nf+1)/2) * (W/nf + 0.29)' ps='2*int((nf+2)/2) * (W/nf + 0.29)' nrd='0.29 / W' nrs='0.29 / W'
+ sa=0 sb=0 sd=0 mult=1 m=1
XM16 Y X net6 VN sky130_fd_pr__nfet_01v8_lvt L=0.15 W=6.5 nf=1 ad='int((nf+1)/2) * W/nf * 0.29' as='int((nf+2)/2) * W/nf * 0.29'
+ pd='2*int((nf+1)/2) * (W/nf + 0.29)' ps='2*int((nf+2)/2) * (W/nf + 0.29)' nrd='0.29 / W' nrs='0.29 / W'
+ sa=0 sb=0 sd=0 mult=1 m=1
XM17 net3 X VN VN sky130_fd_pr__nfet_01v8_lvt L=0.15 W=3.25 nf=1 ad='int((nf+1)/2) * W/nf * 0.29' as='int((nf+2)/2) * W/nf * 0.29'
+ pd='2*int((nf+1)/2) * (W/nf + 0.29)' ps='2*int((nf+2)/2) * (W/nf + 0.29)' nrd='0.29 / W' nrs='0.29 / W'
+ sa=0 sb=0 sd=0 mult=1 m=1
XM18 net2 X VN VN sky130_fd_pr__nfet_01v8_lvt L=0.15 W=1.5 nf=1 ad='int((nf+1)/2) * W/nf * 0.29' as='int((nf+2)/2) * W/nf * 0.29'
+ pd='2*int((nf+1)/2) * (W/nf + 0.29)' ps='2*int((nf+2)/2) * (W/nf + 0.29)' nrd='0.29 / W' nrs='0.29 / W'
+ sa=0 sb=0 sd=0 mult=1 m=1
XM19 net1 X VN VN sky130_fd_pr__nfet_01v8_lvt L=0.15 W=6.5 nf=1 ad='int((nf+1)/2) * W/nf * 0.29' as='int((nf+2)/2) * W/nf * 0.29'
+ pd='2*int((nf+1)/2) * (W/nf + 0.29)' ps='2*int((nf+2)/2) * (W/nf + 0.29)' nrd='0.29 / W' nrs='0.29 / W'
+ sa=0 sb=0 sd=0 mult=1 m=1
XM20 net6 X net1 VN sky130_fd_pr__nfet_01v8_lvt L=0.15 W=6.5 nf=1 ad='int((nf+1)/2) * W/nf * 0.29' as='int((nf+2)/2) * W/nf * 0.29'
+ pd='2*int((nf+1)/2) * (W/nf + 0.29)' ps='2*int((nf+2)/2) * (W/nf + 0.29)' nrd='0.29 / W' nrs='0.29 / W'
+ sa=0 sb=0 sd=0 mult=1 m=1
XM2 net4 X VP VP sky130_fd_pr__pfet_01v8 L=0.15 W=10 nf=1 ad='int((nf+1)/2) * W/nf * 0.29' as='int((nf+2)/2) * W/nf * 0.29'
+ pd='2*int((nf+1)/2) * (W/nf + 0.29)' ps='2*int((nf+2)/2) * (W/nf + 0.29)' nrd='0.29 / W' nrs='0.29 / W'
+ sa=0 sb=0 sd=0 mult=1 m=1
XM5 net5 X net4 net4 sky130_fd_pr__pfet_01v8 L=0.15 W=10 nf=1 ad='int((nf+1)/2) * W/nf * 0.29' as='int((nf+2)/2) * W/nf * 0.29'
+ pd='2*int((nf+1)/2) * (W/nf + 0.29)' ps='2*int((nf+2)/2) * (W/nf + 0.29)' nrd='0.29 / W' nrs='0.29 / W'
+ sa=0 sb=0 sd=0 mult=1 m=1
XM6 Y X net5 VP sky130_fd_pr__pfet_01v8 L=0.15 W=10 nf=1 ad='int((nf+1)/2) * W/nf * 0.29' as='int((nf+2)/2) * W/nf * 0.29'
+ pd='2*int((nf+1)/2) * (W/nf + 0.29)' ps='2*int((nf+2)/2) * (W/nf + 0.29)' nrd='0.29 / W' nrs='0.29 / W'
+ sa=0 sb=0 sd=0 mult=1 m=1
XM8 net3 X VP VP sky130_fd_pr__pfet_01v8 L=0.15 W=2 nf=1 ad='int((nf+1)/2) * W/nf * 0.29' as='int((nf+2)/2) * W/nf * 0.29'
+ pd='2*int((nf+1)/2) * (W/nf + 0.29)' ps='2*int((nf+2)/2) * (W/nf + 0.29)' nrd='0.29 / W' nrs='0.29 / W'
+ sa=0 sb=0 sd=0 mult=1 m=1
XM12 net2 X VP VP sky130_fd_pr__pfet_01v8 L=0.15 W=5 nf=1 ad='int((nf+1)/2) * W/nf * 0.29' as='int((nf+2)/2) * W/nf * 0.29'
+ pd='2*int((nf+1)/2) * (W/nf + 0.29)' ps='2*int((nf+2)/2) * (W/nf + 0.29)' nrd='0.29 / W' nrs='0.29 / W'
+ sa=0 sb=0 sd=0 mult=1 m=1
XM14 net6 X net2 VP sky130_fd_pr__pfet_01v8 L=0.15 W=5 nf=1 ad='int((nf+1)/2) * W/nf * 0.29' as='int((nf+2)/2) * W/nf * 0.29'
+ pd='2*int((nf+1)/2) * (W/nf + 0.29)' ps='2*int((nf+2)/2) * (W/nf + 0.29)' nrd='0.29 / W' nrs='0.29 / W'
+ sa=0 sb=0 sd=0 mult=1 m=1
XM21 net1 X VP VP sky130_fd_pr__pfet_01v8 L=0.15 W=1.5 nf=1 ad='int((nf+1)/2) * W/nf * 0.29' as='int((nf+2)/2) * W/nf * 0.29'
+ pd='2*int((nf+1)/2) * (W/nf + 0.29)' ps='2*int((nf+2)/2) * (W/nf + 0.29)' nrd='0.29 / W' nrs='0.29 / W'
+ sa=0 sb=0 sd=0 mult=1 m=1
.ends

.GLOBAL GND
.end
